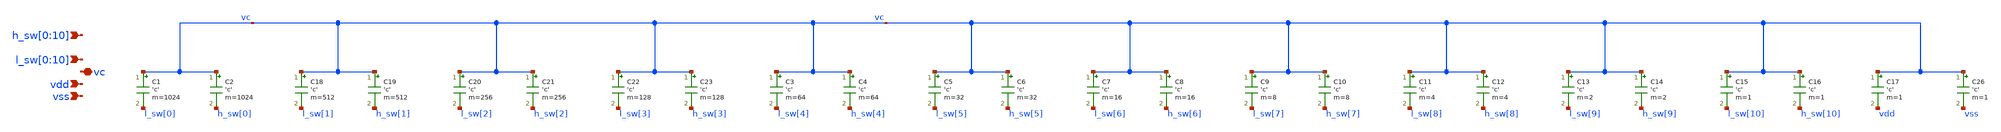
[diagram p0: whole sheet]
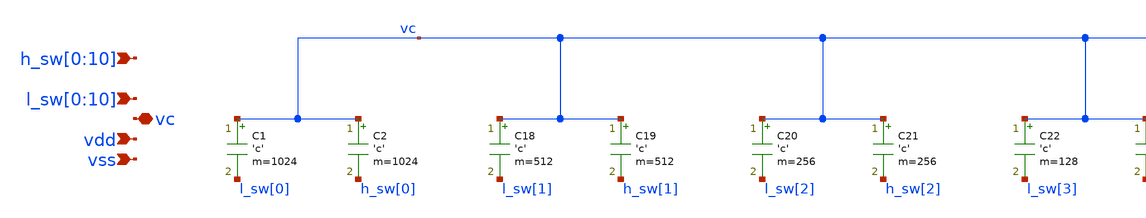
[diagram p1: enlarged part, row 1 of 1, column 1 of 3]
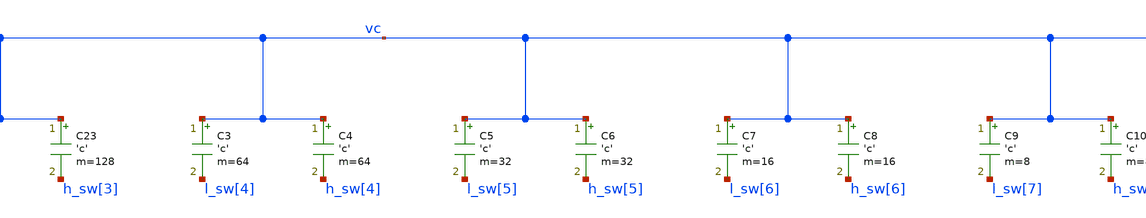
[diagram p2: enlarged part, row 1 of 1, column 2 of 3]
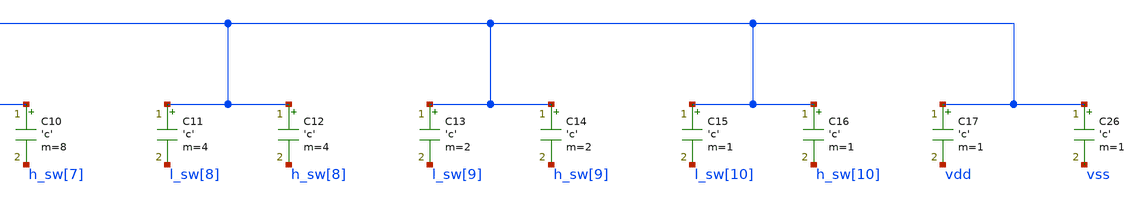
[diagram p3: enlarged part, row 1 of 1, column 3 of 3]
** sch_path: MSPHY9932-main/sch/cap8b.sch
**.subckt cap8b
*+ l_sw[0],l_sw[1],l_sw[2],l_sw[3],l_sw[4],l_sw[5],l_sw[6],l_sw[7],l_sw[8],l_sw[9],l_sw[10] vss vc h_sw[0],h_sw[1],h_sw[2],h_sw[3],h_sw[4],h_sw[5],h_sw[6],h_sw[7],h_sw[8],h_sw[9],h_sw[10] vdd
*.ipin l_sw[0],l_sw[1],l_sw[2],l_sw[3],l_sw[4],l_sw[5],l_sw[6],l_sw[7],l_sw[8],l_sw[9],l_sw[10]
*.ipin vss
*.iopin vc
*.ipin h_sw[0],h_sw[1],h_sw[2],h_sw[3],h_sw[4],h_sw[5],h_sw[6],h_sw[7],h_sw[8],h_sw[9],h_sw[10]
*.ipin vdd
C3 vc l_sw[4] 'c' m=64
C4 vc h_sw[4] 'c' m=64
C5 vc l_sw[5] 'c' m=32
C6 vc h_sw[5] 'c' m=32
C7 vc l_sw[6] 'c' m=16
C8 vc h_sw[6] 'c' m=16
C9 vc l_sw[7] 'c' m=8
C10 vc h_sw[7] 'c' m=8
C11 vc l_sw[8] 'c' m=4
C12 vc h_sw[8] 'c' m=4
C13 vc l_sw[9] 'c' m=2
C14 vc h_sw[9] 'c' m=2
C15 vc l_sw[10] 'c' m=1
C16 vc h_sw[10] 'c' m=1
C17 vc vdd 'c' m=1
C26 vc vss 'c' m=1
C1 vc l_sw[0] 'c' m=1024
C2 vc h_sw[0] 'c' m=1024
C18 vc l_sw[1] 'c' m=512
C19 vc h_sw[1] 'c' m=512
C20 vc l_sw[2] 'c' m=256
C21 vc h_sw[2] 'c' m=256
C22 vc l_sw[3] 'c' m=128
C23 vc h_sw[3] 'c' m=128
**.ends
.end
